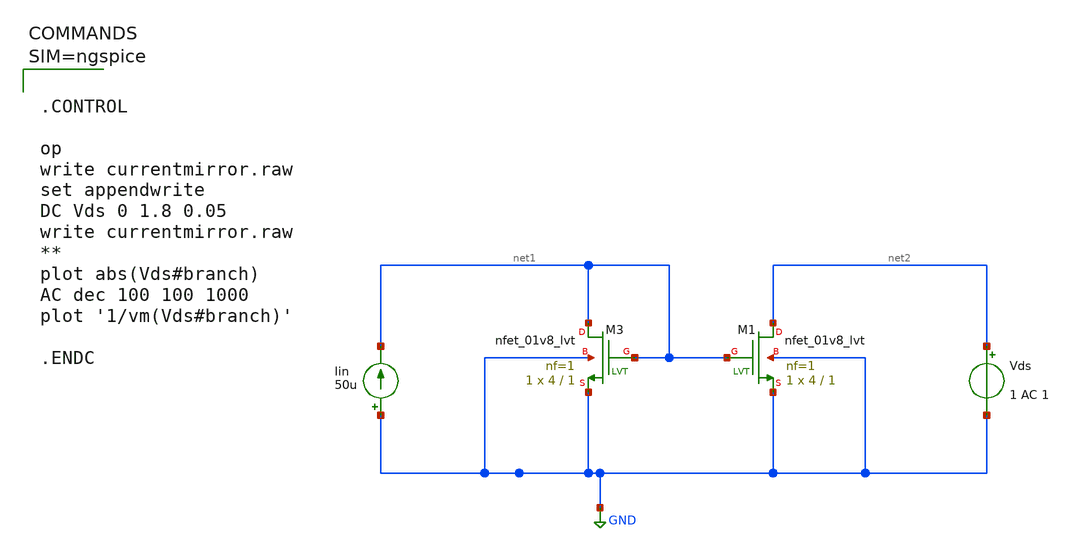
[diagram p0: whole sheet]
** sch_path: work/xschem/currentmirror.sch
**.subckt currentmirror
XM1 net2 net1 GND GND sky130_fd_pr__nfet_01v8_lvt L=1 W=4 nf=1 ad='int((1 + 1)/2) * 4 / 1 * 0.29' as='int((1 + 2)/2) * 4 / 1 * 0.29'
+ pd='2*int((1 + 1)/2) * (4 / 1 + 0.29)' ps='2*int((1 + 2)/2) * (4 / 1 + 0.29)' nrd='0.29 / 4 ' nrs='0.29 / 4 '
+ sa=0 sb=0 sd=0 mult=1 m=1
Iin GND net1 50u
Vds net2 GND 1 AC 1
XM3 net1 net1 GND GND sky130_fd_pr__nfet_01v8_lvt L=1 W=4 nf=1 ad='int((1 + 1)/2) * 4 / 1 * 0.29' as='int((1 + 2)/2) * 4 / 1 * 0.29'
+ pd='2*int((1 + 1)/2) * (4 / 1 + 0.29)' ps='2*int((1 + 2)/2) * (4 / 1 + 0.29)' nrd='0.29 / 4 ' nrs='0.29 / 4 '
+ sa=0 sb=0 sd=0 mult=1 m=1
**** begin user architecture code



.CONTROL

op
write currentmirror.raw
set appendwrite
DC Vds 0 1.8 0.05
write currentmirror.raw
**
plot abs(Vds#branch)
AC dec 100 100 1000
plot '1/vm(Vds#branch)'

.ENDC





** opencircuitdesign pdks install
.lib $::SKYWATER_MODELS/sky130.lib.spice tt

**** end user architecture code
**.ends
.GLOBAL GND
.end
